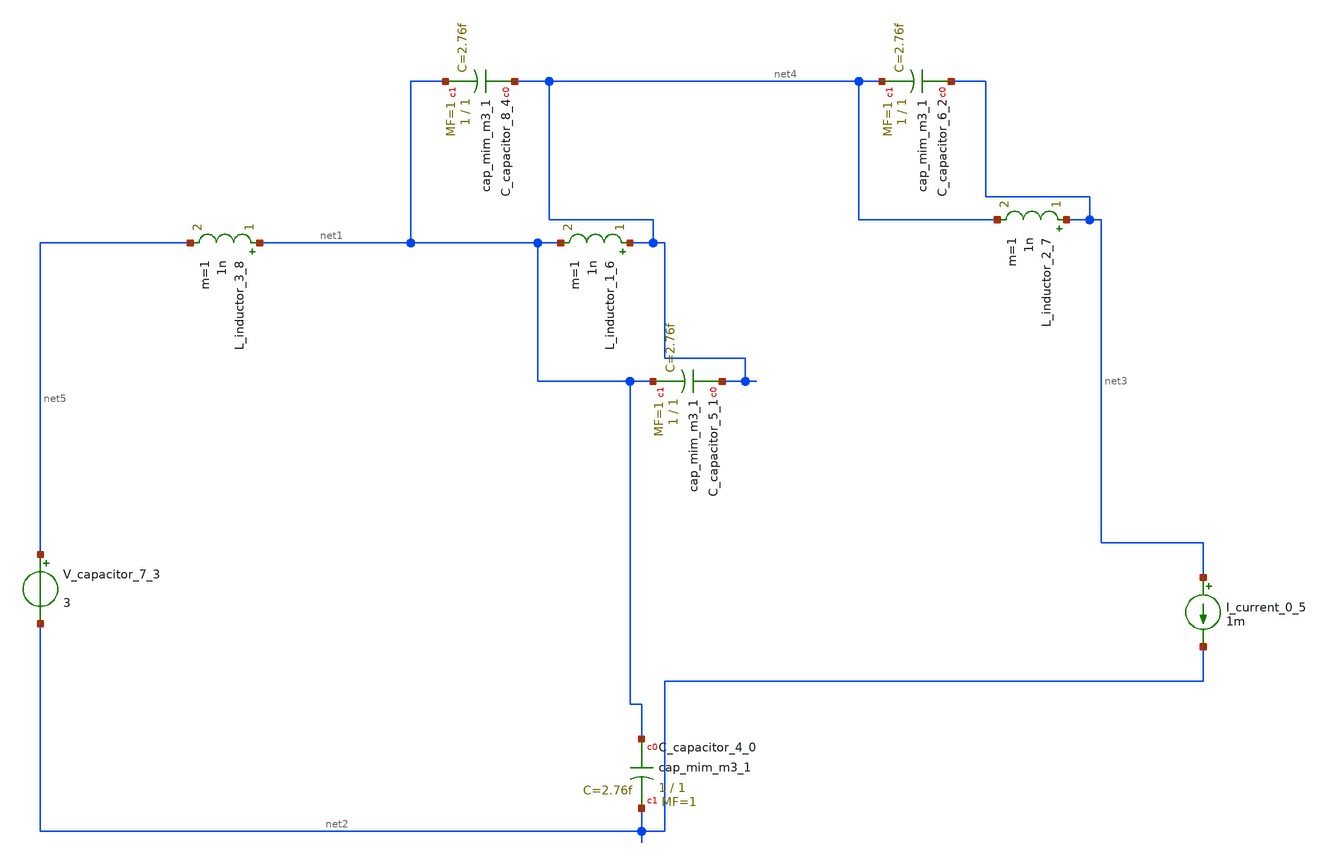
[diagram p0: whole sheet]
** sch_path: schematics/SchemGen/10_1109_ACCESS_2019_2959136_04_002.sch
**.subckt 10_1109_ACCESS_2019_2959136_04_002
XC_capacitor_4_0 net1 net2 sky130_fd_pr__cap_mim_m3_1 W=1 L=1 MF=1 m=1
XC_capacitor_5_1 net4 net1 sky130_fd_pr__cap_mim_m3_1 W=1 L=1 MF=1 m=1
XC_capacitor_6_2 net3 net4 sky130_fd_pr__cap_mim_m3_1 W=1 L=1 MF=1 m=1
V_capacitor_7_3 net5 net2 3
XC_capacitor_8_4 net4 net1 sky130_fd_pr__cap_mim_m3_1 W=1 L=1 MF=1 m=1
I_current_0_5 net3 net2 1m
L_inductor_1_6 net4 net1 1n m=1
L_inductor_2_7 net3 net4 1n m=1
L_inductor_3_8 net1 net5 1n m=1
**.ends
.end
